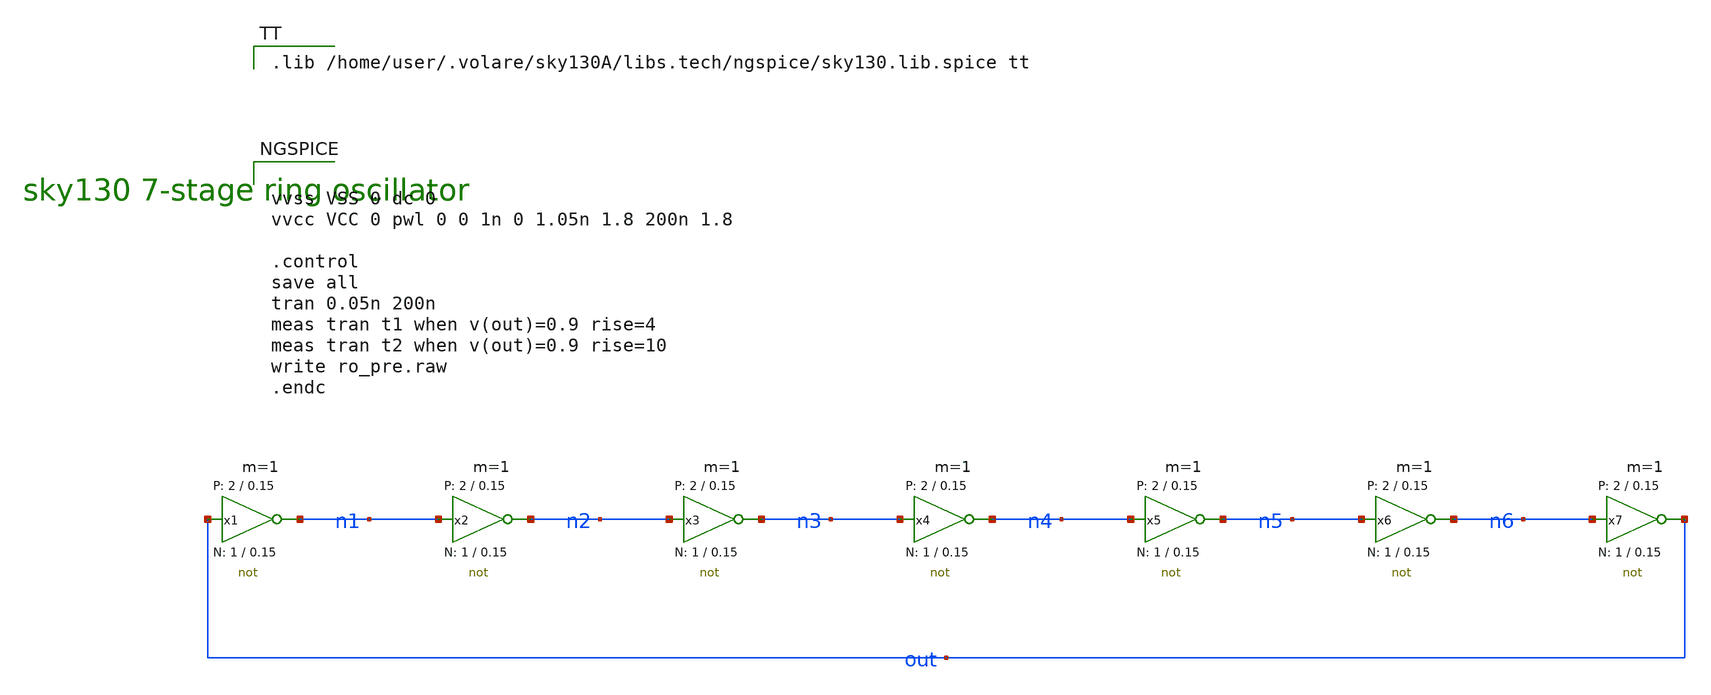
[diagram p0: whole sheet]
** sch_path: ro/netlist/ro.sch
* StefanSchippers/xschem_sky130/sky130_tests/not.sch:
* Copyright 2021 Stefan Frederik Schippers
* Licensed under the Apache License, Version 2.0 (the "License");
**.subckt ro
x1 n1 out VCC VSS not W_N=1 L_N=0.15 W_P=2 L_P=0.15 m=1
x2 n2 n1 VCC VSS not W_N=1 L_N=0.15 W_P=2 L_P=0.15 m=1
x3 n3 n2 VCC VSS not W_N=1 L_N=0.15 W_P=2 L_P=0.15 m=1
x4 n4 n3 VCC VSS not W_N=1 L_N=0.15 W_P=2 L_P=0.15 m=1
x5 n5 n4 VCC VSS not W_N=1 L_N=0.15 W_P=2 L_P=0.15 m=1
x6 n6 n5 VCC VSS not W_N=1 L_N=0.15 W_P=2 L_P=0.15 m=1
x7 out n6 VCC VSS not W_N=1 L_N=0.15 W_P=2 L_P=0.15 m=1
**** begin user architecture code

.lib /home/user/.volare/sky130A/libs.tech/ngspice/sky130.lib.spice tt



vvss VSS 0 dc 0
vvcc VCC 0 pwl 0 0 1n 0 1.05n 1.8 200n 1.8

.control
save all
tran 0.05n 200n
meas tran t1 when v(out)=0.9 rise=4
meas tran t2 when v(out)=0.9 rise=10
write ro_pre.raw
.endc


**** end user architecture code
**.ends

* expanding   symbol:  sky130_tests/not.sym # of pins=2
** sym_path: sky130_tests/not.sym
** sch_path: sky130_tests/not.sch
.subckt not y a VCCPIN VSSPIN     W_N=1 L_N=0.15 W_P=2 L_P=0.15
*.opin y
*.ipin a
XM1 DN a VSSPIN VSSPIN sky130_fd_pr__nfet_01v8 L=L_N W=W_N nf=1 ad='int((1 + 1)/2) * W_N / 1 * 0.29'
+ as='int((1 + 2)/2) * W_N / 1 * 0.29' pd='2*int((1 + 1)/2) * (W_N / 1 + 0.29)' ps='2*int((1 + 2)/2) * (W_N / 1 + 0.29)'
+ nrd='0.29 / W_N ' nrs='0.29 / W_N ' sa=0 sb=0 sd=0 mult=1 m=1
XM2 DP a VCCPIN VCCPIN sky130_fd_pr__pfet_01v8 L=L_P W=W_P nf=1 ad='int((nf+1)/2) * W/nf * 0.29' as='int((nf+2)/2) * W/nf * 0.29'
+ pd='2*int((nf+1)/2) * (W/nf + 0.29)' ps='2*int((nf+2)/2) * (W/nf + 0.29)' nrd='0.29 / W' nrs='0.29 / W'
+ sa=0 sb=0 sd=0 mult=1 m=1
Vmeas DP y 0
.save i(vmeas)
Vmeas1 y DN 0
.save i(vmeas1)
.save v(dp)
.save v(dn)
.ends

.end
